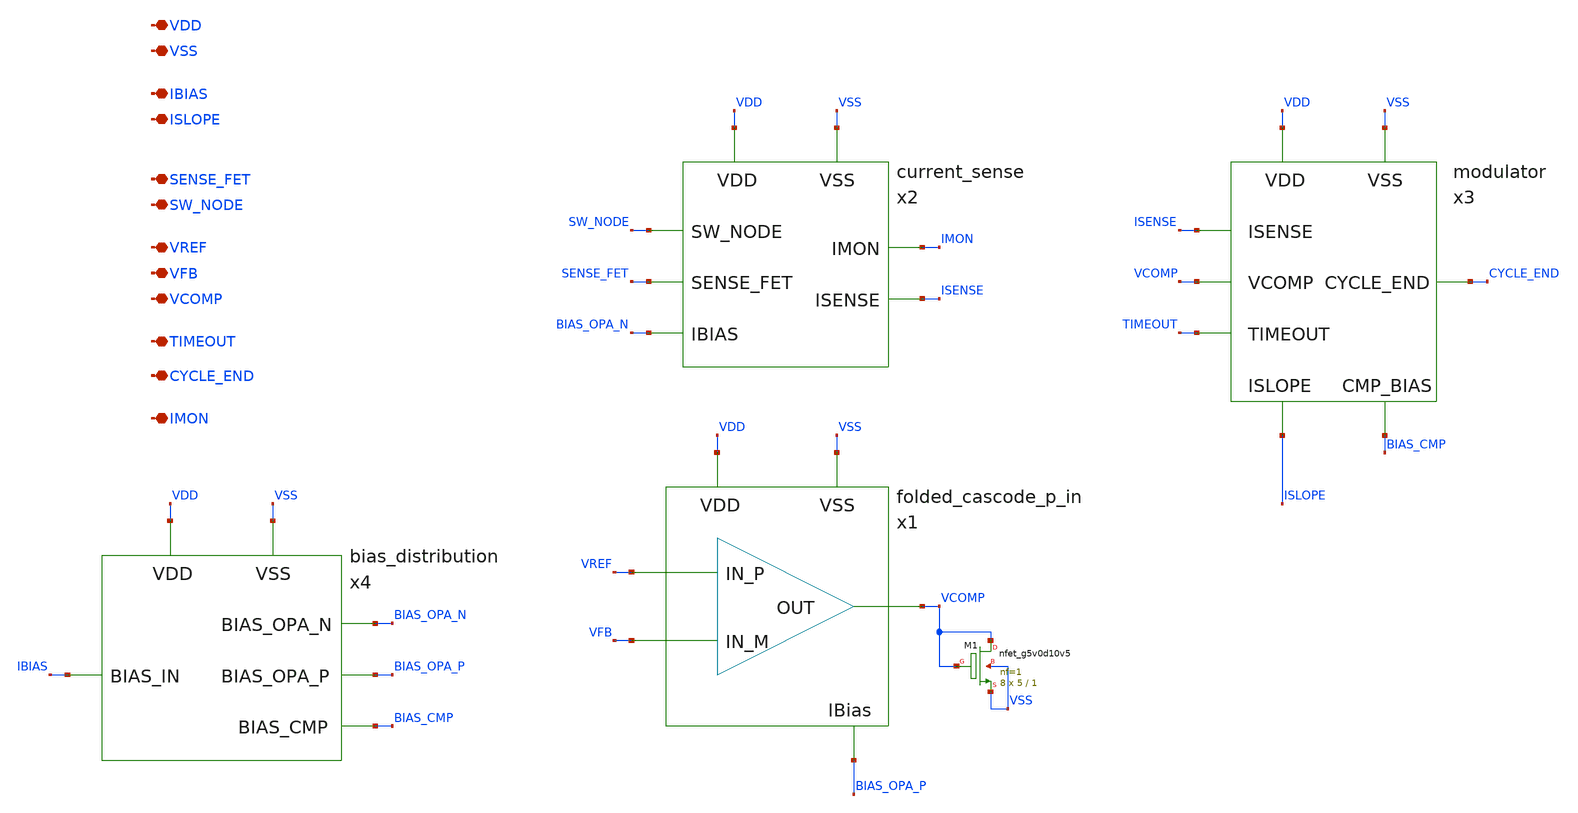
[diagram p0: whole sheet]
** sch_path: design/system/analog_subsystem.sch
**.subckt analog_subsystem VDD VSS IBIAS SENSE_FET SW_NODE ISLOPE VREF VFB VCOMP TIMEOUT CYCLE_END
*+ IMON
*.iopin VDD
*.iopin VSS
*.iopin IBIAS
*.iopin SENSE_FET
*.iopin SW_NODE
*.iopin ISLOPE
*.iopin VREF
*.iopin VFB
*.iopin VCOMP
*.iopin TIMEOUT
*.iopin CYCLE_END
*.iopin IMON
x1 VREF VFB VCOMP VDD VSS BIAS_OPA_P folded_cascode_p_in
x2 VDD VSS SW_NODE SENSE_FET BIAS_OPA_N IMON ISENSE current_sense
x3 VDD VSS BIAS_CMP ISLOPE ISENSE VCOMP TIMEOUT CYCLE_END modulator
x4 VDD VSS IBIAS BIAS_OPA_N BIAS_OPA_P BIAS_CMP bias_distribution
XM1 VCOMP VCOMP VSS VSS sky130_fd_pr__nfet_g5v0d10v5 L=1 W=5 nf=1 ad='int((nf+1)/2) * W/nf * 0.29' as='int((nf+2)/2) * W/nf * 0.29'
+ pd='2*int((nf+1)/2) * (W/nf + 0.29)' ps='2*int((nf+2)/2) * (W/nf + 0.29)' nrd='0.29 / W' nrs='0.29 / W'
+ sa=0 sb=0 sd=0 mult=8 m=8
**.ends

* expanding   symbol:  design/folded-cascode-p-in/folded_cascode_p_in.sym # of pins=6
** sym_path: design/folded-cascode-p-in/folded_cascode_p_in.sym
** sch_path: design/folded-cascode-p-in/folded_cascode_p_in.sch
.subckt folded_cascode_p_in IN_P IN_M OUT VDD VSS VBN
*.ipin IN_P
*.ipin IN_M
*.ipin OUT
*.ipin VDD
*.ipin VSS
*.ipin VBN
XM7 net4 VBP VDD VDD sky130_fd_pr__pfet_g5v0d10v5 L=1 W=5 nf=1 ad='int((nf+1)/2) * W/nf * 0.29' as='int((nf+2)/2) * W/nf * 0.29'
+ pd='2*int((nf+1)/2) * (W/nf + 0.29)' ps='2*int((nf+2)/2) * (W/nf + 0.29)' nrd='0.29 / W' nrs='0.29 / W'
+ sa=0 sb=0 sd=0 mult=12 m=12
XM8 VS1_P IN_M net4 VDD sky130_fd_pr__pfet_g5v0d10v5 L=1 W=5 nf=1 ad='int((nf+1)/2) * W/nf * 0.29' as='int((nf+2)/2) * W/nf * 0.29'
+ pd='2*int((nf+1)/2) * (W/nf + 0.29)' ps='2*int((nf+2)/2) * (W/nf + 0.29)' nrd='0.29 / W' nrs='0.29 / W'
+ sa=0 sb=0 sd=0 mult=24 m=24
XM15 VS1_M IN_P net4 VDD sky130_fd_pr__pfet_g5v0d10v5 L=1 W=5 nf=1 ad='int((nf+1)/2) * W/nf * 0.29' as='int((nf+2)/2) * W/nf * 0.29'
+ pd='2*int((nf+1)/2) * (W/nf + 0.29)' ps='2*int((nf+2)/2) * (W/nf + 0.29)' nrd='0.29 / W' nrs='0.29 / W'
+ sa=0 sb=0 sd=0 mult=24 m=24
XM16 VS1_P VBN_INT VSS VSS sky130_fd_pr__nfet_g5v0d10v5 L=1 W=5 nf=1 ad='int((nf+1)/2) * W/nf * 0.29'
+ as='int((nf+2)/2) * W/nf * 0.29' pd='2*int((nf+1)/2) * (W/nf + 0.29)' ps='2*int((nf+2)/2) * (W/nf + 0.29)'
+ nrd='0.29 / W' nrs='0.29 / W' sa=0 sb=0 sd=0 mult=10 m=10
XM20 VS1_M VBN_INT VSS VSS sky130_fd_pr__nfet_g5v0d10v5 L=1 W=5 nf=1 ad='int((nf+1)/2) * W/nf * 0.29'
+ as='int((nf+2)/2) * W/nf * 0.29' pd='2*int((nf+1)/2) * (W/nf + 0.29)' ps='2*int((nf+2)/2) * (W/nf + 0.29)'
+ nrd='0.29 / W' nrs='0.29 / W' sa=0 sb=0 sd=0 mult=10 m=10
XM22 net3 VCP net1 VDD sky130_fd_pr__pfet_g5v0d10v5 L=1 W=5 nf=1 ad='int((nf+1)/2) * W/nf * 0.29' as='int((nf+2)/2) * W/nf * 0.29'
+ pd='2*int((nf+1)/2) * (W/nf + 0.29)' ps='2*int((nf+2)/2) * (W/nf + 0.29)' nrd='0.29 / W' nrs='0.29 / W'
+ sa=0 sb=0 sd=0 mult=4 m=4
XM23 net1 net3 VDD VDD sky130_fd_pr__pfet_g5v0d10v5 L=1 W=5 nf=1 ad='int((nf+1)/2) * W/nf * 0.29' as='int((nf+2)/2) * W/nf * 0.29'
+ pd='2*int((nf+1)/2) * (W/nf + 0.29)' ps='2*int((nf+2)/2) * (W/nf + 0.29)' nrd='0.29 / W' nrs='0.29 / W'
+ sa=0 sb=0 sd=0 mult=4 m=4
XM24 OUT VCP net2 VDD sky130_fd_pr__pfet_g5v0d10v5 L=1 W=5 nf=1 ad='int((nf+1)/2) * W/nf * 0.29' as='int((nf+2)/2) * W/nf * 0.29'
+ pd='2*int((nf+1)/2) * (W/nf + 0.29)' ps='2*int((nf+2)/2) * (W/nf + 0.29)' nrd='0.29 / W' nrs='0.29 / W'
+ sa=0 sb=0 sd=0 mult=4 m=4
XM25 net2 net3 VDD VDD sky130_fd_pr__pfet_g5v0d10v5 L=1 W=5 nf=1 ad='int((nf+1)/2) * W/nf * 0.29' as='int((nf+2)/2) * W/nf * 0.29'
+ pd='2*int((nf+1)/2) * (W/nf + 0.29)' ps='2*int((nf+2)/2) * (W/nf + 0.29)' nrd='0.29 / W' nrs='0.29 / W'
+ sa=0 sb=0 sd=0 mult=4 m=4
XM26 OUT VCN VS1_P VSS sky130_fd_pr__nfet_g5v0d10v5 L=1 W=5 nf=1 ad='int((nf+1)/2) * W/nf * 0.29' as='int((nf+2)/2) * W/nf * 0.29'
+ pd='2*int((nf+1)/2) * (W/nf + 0.29)' ps='2*int((nf+2)/2) * (W/nf + 0.29)' nrd='0.29 / W' nrs='0.29 / W'
+ sa=0 sb=0 sd=0 mult=4 m=4
XM27 net3 VCN VS1_M VSS sky130_fd_pr__nfet_g5v0d10v5 L=1 W=5 nf=1 ad='int((nf+1)/2) * W/nf * 0.29' as='int((nf+2)/2) * W/nf * 0.29'
+ pd='2*int((nf+1)/2) * (W/nf + 0.29)' ps='2*int((nf+2)/2) * (W/nf + 0.29)' nrd='0.29 / W' nrs='0.29 / W'
+ sa=0 sb=0 sd=0 mult=4 m=4
XM29 VBN_INT VBN_INT VSS VSS sky130_fd_pr__nfet_g5v0d10v5 L=1 W=5 nf=1 ad='int((nf+1)/2) * W/nf * 0.29'
+ as='int((nf+2)/2) * W/nf * 0.29' pd='2*int((nf+1)/2) * (W/nf + 0.29)' ps='2*int((nf+2)/2) * (W/nf + 0.29)'
+ nrd='0.29 / W' nrs='0.29 / W' sa=0 sb=0 sd=0 mult=1 m=1
XM30 VBN_INT VBP VDD VDD sky130_fd_pr__pfet_g5v0d10v5 L=1 W=5 nf=1 ad='int((nf+1)/2) * W/nf * 0.29' as='int((nf+2)/2) * W/nf * 0.29'
+ pd='2*int((nf+1)/2) * (W/nf + 0.29)' ps='2*int((nf+2)/2) * (W/nf + 0.29)' nrd='0.29 / W' nrs='0.29 / W'
+ sa=0 sb=0 sd=0 mult=1 m=1
XM14 VBN_INT VBN_INT VS1_P VDD sky130_fd_pr__pfet_g5v0d10v5 L=1 W=5 nf=1 ad='int((nf+1)/2) * W/nf * 0.29'
+ as='int((nf+2)/2) * W/nf * 0.29' pd='2*int((nf+1)/2) * (W/nf + 0.29)' ps='2*int((nf+2)/2) * (W/nf + 0.29)'
+ nrd='0.29 / W' nrs='0.29 / W' sa=0 sb=0 sd=0 mult=1 m=1
XM17 VBN_INT VBN_INT VS1_M VDD sky130_fd_pr__pfet_g5v0d10v5 L=1 W=5 nf=1 ad='int((nf+1)/2) * W/nf * 0.29'
+ as='int((nf+2)/2) * W/nf * 0.29' pd='2*int((nf+1)/2) * (W/nf + 0.29)' ps='2*int((nf+2)/2) * (W/nf + 0.29)'
+ nrd='0.29 / W' nrs='0.29 / W' sa=0 sb=0 sd=0 mult=1 m=1
x1 VBN VCN VBP VCP VDD VSS cascode_bias
.ends


* expanding   symbol:  design/current-sense/current_sense.sym # of pins=7
** sym_path: design/current-sense/current_sense.sym
** sch_path: design/current-sense/current_sense.sch
.subckt current_sense VDD VSS SW_NODE SENSE_FET IBIAS IMON ISENSE
*.ipin SW_NODE
*.ipin SENSE_FET
*.ipin VDD
*.ipin VSS
*.ipin IBIAS
*.ipin IMON
*.ipin ISENSE
x1 SW_NODE SENSE_FET OPA_OUT VDD VSS IBIAS folded_cascode_n_in
XM1 net1 OPA_OUT SENSE_FET VDD sky130_fd_pr__pfet_g5v0d10v5 L=1 W=5 nf=1 ad='int((nf+1)/2) * W/nf * 0.29'
+ as='int((nf+2)/2) * W/nf * 0.29' pd='2*int((nf+1)/2) * (W/nf + 0.29)' ps='2*int((nf+2)/2) * (W/nf + 0.29)'
+ nrd='0.29 / W' nrs='0.29 / W' sa=0 sb=0 sd=0 mult=20 m=20
XM2 net1 net1 VSS VSS sky130_fd_pr__nfet_g5v0d10v5 L=1 W=5 nf=1 ad='int((nf+1)/2) * W/nf * 0.29' as='int((nf+2)/2) * W/nf * 0.29'
+ pd='2*int((nf+1)/2) * (W/nf + 0.29)' ps='2*int((nf+2)/2) * (W/nf + 0.29)' nrd='0.29 / W' nrs='0.29 / W'
+ sa=0 sb=0 sd=0 mult=20 m=20
XM4 net2 net1 VSS VSS sky130_fd_pr__nfet_g5v0d10v5 L=1 W=5 nf=1 ad='int((nf+1)/2) * W/nf * 0.29' as='int((nf+2)/2) * W/nf * 0.29'
+ pd='2*int((nf+1)/2) * (W/nf + 0.29)' ps='2*int((nf+2)/2) * (W/nf + 0.29)' nrd='0.29 / W' nrs='0.29 / W'
+ sa=0 sb=0 sd=0 mult=8 m=8
XM3 net2 net2 VDD VDD sky130_fd_pr__pfet_g5v0d10v5 L=1 W=5 nf=1 ad='int((nf+1)/2) * W/nf * 0.29' as='int((nf+2)/2) * W/nf * 0.29'
+ pd='2*int((nf+1)/2) * (W/nf + 0.29)' ps='2*int((nf+2)/2) * (W/nf + 0.29)' nrd='0.29 / W' nrs='0.29 / W'
+ sa=0 sb=0 sd=0 mult=8 m=8
XM5 I_MON net1 VSS VSS sky130_fd_pr__nfet_g5v0d10v5 L=1 W=5 nf=1 ad='int((nf+1)/2) * W/nf * 0.29' as='int((nf+2)/2) * W/nf * 0.29'
+ pd='2*int((nf+1)/2) * (W/nf + 0.29)' ps='2*int((nf+2)/2) * (W/nf + 0.29)' nrd='0.29 / W' nrs='0.29 / W'
+ sa=0 sb=0 sd=0 mult=20 m=20
XM6 ISENSE net2 VDD VDD sky130_fd_pr__pfet_g5v0d10v5 L=1 W=5 nf=1 ad='int((nf+1)/2) * W/nf * 0.29' as='int((nf+2)/2) * W/nf * 0.29'
+ pd='2*int((nf+1)/2) * (W/nf + 0.29)' ps='2*int((nf+2)/2) * (W/nf + 0.29)' nrd='0.29 / W' nrs='0.29 / W'
+ sa=0 sb=0 sd=0 mult=4 m=4
XR6 VSS ISENSE VSS sky130_fd_pr__res_high_po_1p41 L=20 mult=1 m=1
XR1 VSS ISENSE VSS sky130_fd_pr__res_high_po_1p41 L=20 mult=1 m=1
.ends


* expanding   symbol:  design/modulator/modulator.sym # of pins=8
** sym_path: design/modulator/modulator.sym
** sch_path: design/modulator/modulator.sch
.subckt modulator VDD VSS CMP_BIAS ISLOPE ISENSE VCOMP TIMEOUT CYCLE_END
*.ipin ISENSE
*.ipin VCOMP
*.ipin TIMEOUT
*.ipin VDD
*.ipin VSS
*.ipin CMP_BIAS
*.ipin ISLOPE
*.ipin CYCLE_END
x1 IMOD VCOMP CYCLE_END VDD VSS CMP_BIAS comparator_w_obuff
XM10 IMOD net1 VDD VDD sky130_fd_pr__pfet_g5v0d10v5 L=2 W=5 nf=1 ad='int((nf+1)/2) * W/nf * 0.29' as='int((nf+2)/2) * W/nf * 0.29'
+ pd='2*int((nf+1)/2) * (W/nf + 0.29)' ps='2*int((nf+2)/2) * (W/nf + 0.29)' nrd='0.29 / W' nrs='0.29 / W'
+ sa=0 sb=0 sd=0 mult=2 m=2
XM11 net1 net1 VDD VDD sky130_fd_pr__pfet_g5v0d10v5 L=2 W=5 nf=1 ad='int((nf+1)/2) * W/nf * 0.29' as='int((nf+2)/2) * W/nf * 0.29'
+ pd='2*int((nf+1)/2) * (W/nf + 0.29)' ps='2*int((nf+2)/2) * (W/nf + 0.29)' nrd='0.29 / W' nrs='0.29 / W'
+ sa=0 sb=0 sd=0 mult=12 m=12
XM12 ISENSE TIMEOUT VSS VSS sky130_fd_pr__nfet_g5v0d10v5 L=1 W=5 nf=1 ad='int((nf+1)/2) * W/nf * 0.29'
+ as='int((nf+2)/2) * W/nf * 0.29' pd='2*int((nf+1)/2) * (W/nf + 0.29)' ps='2*int((nf+2)/2) * (W/nf + 0.29)'
+ nrd='0.29 / W' nrs='0.29 / W' sa=0 sb=0 sd=0 mult=4 m=4
XM13 IMOD TIMEOUT ISENSE GND sky130_fd_pr__nfet_g5v0d10v5 L=1 W=5 nf=1 ad='int((nf+1)/2) * W/nf * 0.29'
+ as='int((nf+2)/2) * W/nf * 0.29' pd='2*int((nf+1)/2) * (W/nf + 0.29)' ps='2*int((nf+2)/2) * (W/nf + 0.29)'
+ nrd='0.29 / W' nrs='0.29 / W' sa=0 sb=0 sd=0 mult=1 m=1
XC4 IMOD ISENSE sky130_fd_pr__cap_mim_m3_1 W=30 L=30 MF=1 m=1
XC6 IMOD ISENSE sky130_fd_pr__cap_mim_m3_2 W=30 L=30 MF=1 m=1
XM1 net1 ISLOPE VSS VSS sky130_fd_pr__nfet_g5v0d10v5 L=1 W=5 nf=1 ad='int((nf+1)/2) * W/nf * 0.29' as='int((nf+2)/2) * W/nf * 0.29'
+ pd='2*int((nf+1)/2) * (W/nf + 0.29)' ps='2*int((nf+2)/2) * (W/nf + 0.29)' nrd='0.29 / W' nrs='0.29 / W'
+ sa=0 sb=0 sd=0 mult=1 m=1
XM2 ISLOPE ISLOPE VSS VSS sky130_fd_pr__nfet_g5v0d10v5 L=1 W=5 nf=1 ad='int((nf+1)/2) * W/nf * 0.29'
+ as='int((nf+2)/2) * W/nf * 0.29' pd='2*int((nf+1)/2) * (W/nf + 0.29)' ps='2*int((nf+2)/2) * (W/nf + 0.29)'
+ nrd='0.29 / W' nrs='0.29 / W' sa=0 sb=0 sd=0 mult=4 m=4
.ends


* expanding   symbol:  design/bias-circuit/bias_distribution.sym # of pins=6
** sym_path: design/bias-circuit/bias_distribution.sym
** sch_path: design/bias-circuit/bias_distribution.sch
.subckt bias_distribution VDD VSS BIAS_IN BIAS_OPA_N BIAS_OPA_P BIAS_CMP
*.ipin BIAS_OPA_P
*.ipin VSS
*.ipin VDD
*.ipin BIAS_IN
*.ipin BIAS_OPA_N
*.ipin BIAS_CMP
XM10 net1 net1 VDD VDD sky130_fd_pr__pfet_g5v0d10v5 L=2 W=5 nf=1 ad='int((nf+1)/2) * W/nf * 0.29' as='int((nf+2)/2) * W/nf * 0.29'
+ pd='2*int((nf+1)/2) * (W/nf + 0.29)' ps='2*int((nf+2)/2) * (W/nf + 0.29)' nrd='0.29 / W' nrs='0.29 / W'
+ sa=0 sb=0 sd=0 mult=2 m=2
XM13 BIAS_IN BIAS_IN VSS VSS sky130_fd_pr__nfet_g5v0d10v5 L=2 W=5 nf=1 ad='int((nf+1)/2) * W/nf * 0.29'
+ as='int((nf+2)/2) * W/nf * 0.29' pd='2*int((nf+1)/2) * (W/nf + 0.29)' ps='2*int((nf+2)/2) * (W/nf + 0.29)'
+ nrd='0.29 / W' nrs='0.29 / W' sa=0 sb=0 sd=0 mult=10 m=10
XM1 BIAS_CMP BIAS_IN VSS VSS sky130_fd_pr__nfet_g5v0d10v5 L=2 W=5 nf=1 ad='int((nf+1)/2) * W/nf * 0.29'
+ as='int((nf+2)/2) * W/nf * 0.29' pd='2*int((nf+1)/2) * (W/nf + 0.29)' ps='2*int((nf+2)/2) * (W/nf + 0.29)'
+ nrd='0.29 / W' nrs='0.29 / W' sa=0 sb=0 sd=0 mult=2 m=2
XM2 net1 BIAS_IN VSS VSS sky130_fd_pr__nfet_g5v0d10v5 L=2 W=5 nf=1 ad='int((nf+1)/2) * W/nf * 0.29' as='int((nf+2)/2) * W/nf * 0.29'
+ pd='2*int((nf+1)/2) * (W/nf + 0.29)' ps='2*int((nf+2)/2) * (W/nf + 0.29)' nrd='0.29 / W' nrs='0.29 / W'
+ sa=0 sb=0 sd=0 mult=2 m=2
XM3 BIAS_OPA_N net1 VDD VDD sky130_fd_pr__pfet_g5v0d10v5 L=2 W=5 nf=1 ad='int((nf+1)/2) * W/nf * 0.29'
+ as='int((nf+2)/2) * W/nf * 0.29' pd='2*int((nf+1)/2) * (W/nf + 0.29)' ps='2*int((nf+2)/2) * (W/nf + 0.29)'
+ nrd='0.29 / W' nrs='0.29 / W' sa=0 sb=0 sd=0 mult=2 m=2
XM4 BIAS_OPA_P net1 VDD VDD sky130_fd_pr__pfet_g5v0d10v5 L=2 W=5 nf=1 ad='int((nf+1)/2) * W/nf * 0.29'
+ as='int((nf+2)/2) * W/nf * 0.29' pd='2*int((nf+1)/2) * (W/nf + 0.29)' ps='2*int((nf+2)/2) * (W/nf + 0.29)'
+ nrd='0.29 / W' nrs='0.29 / W' sa=0 sb=0 sd=0 mult=2 m=2
.ends


* expanding   symbol:  design/bias-circuit/cascode_bias.sym # of pins=6
** sym_path: design/bias-circuit/cascode_bias.sym
** sch_path: design/bias-circuit/cascode_bias.sch
.subckt cascode_bias VBN VCN VBP VCP VDD VSS
*.ipin VCN
*.ipin VBP
*.ipin VCP
*.ipin VDD
*.ipin VSS
*.ipin VBN
XM1 VBP VBP VDD VDD sky130_fd_pr__pfet_g5v0d10v5 L=1 W=5 nf=1 ad='int((nf+1)/2) * W/nf * 0.29' as='int((nf+2)/2) * W/nf * 0.29'
+ pd='2*int((nf+1)/2) * (W/nf + 0.29)' ps='2*int((nf+2)/2) * (W/nf + 0.29)' nrd='0.29 / W' nrs='0.29 / W'
+ sa=0 sb=0 sd=0 mult=1 m=1
XM2 net1 VBP net8 VDD sky130_fd_pr__pfet_g5v0d10v5 L=1 W=5 nf=1 ad='int((nf+1)/2) * W/nf * 0.29' as='int((nf+2)/2) * W/nf * 0.29'
+ pd='2*int((nf+1)/2) * (W/nf + 0.29)' ps='2*int((nf+2)/2) * (W/nf + 0.29)' nrd='0.29 / W' nrs='0.29 / W'
+ sa=0 sb=0 sd=0 mult=1 m=1
XM3 VCN VBP VDD VDD sky130_fd_pr__pfet_g5v0d10v5 L=1 W=5 nf=1 ad='int((nf+1)/2) * W/nf * 0.29' as='int((nf+2)/2) * W/nf * 0.29'
+ pd='2*int((nf+1)/2) * (W/nf + 0.29)' ps='2*int((nf+2)/2) * (W/nf + 0.29)' nrd='0.29 / W' nrs='0.29 / W'
+ sa=0 sb=0 sd=0 mult=1 m=1
XM4 net1 net1 net2 VSS sky130_fd_pr__nfet_g5v0d10v5 L=1 W=5 nf=1 ad='int((nf+1)/2) * W/nf * 0.29' as='int((nf+2)/2) * W/nf * 0.29'
+ pd='2*int((nf+1)/2) * (W/nf + 0.29)' ps='2*int((nf+2)/2) * (W/nf + 0.29)' nrd='0.29 / W' nrs='0.29 / W'
+ sa=0 sb=0 sd=0 mult=2 m=2
XM5 net2 net1 VSS VSS sky130_fd_pr__nfet_g5v0d10v5 L=1 W=5 nf=1 ad='int((nf+1)/2) * W/nf * 0.29' as='int((nf+2)/2) * W/nf * 0.29'
+ pd='2*int((nf+1)/2) * (W/nf + 0.29)' ps='2*int((nf+2)/2) * (W/nf + 0.29)' nrd='0.29 / W' nrs='0.29 / W'
+ sa=0 sb=0 sd=0 mult=1 m=1
XM21 VCN VCN net2 VSS sky130_fd_pr__nfet_g5v0d10v5 L=1 W=5 nf=1 ad='int((nf+1)/2) * W/nf * 0.29' as='int((nf+2)/2) * W/nf * 0.29'
+ pd='2*int((nf+1)/2) * (W/nf + 0.29)' ps='2*int((nf+2)/2) * (W/nf + 0.29)' nrd='0.29 / W' nrs='0.29 / W'
+ sa=0 sb=0 sd=0 mult=1 m=1
XM6 net3 VBN net6 VSS sky130_fd_pr__nfet_g5v0d10v5 L=1 W=5 nf=1 ad='int((nf+1)/2) * W/nf * 0.29' as='int((nf+2)/2) * W/nf * 0.29'
+ pd='2*int((nf+1)/2) * (W/nf + 0.29)' ps='2*int((nf+2)/2) * (W/nf + 0.29)' nrd='0.29 / W' nrs='0.29 / W'
+ sa=0 sb=0 sd=0 mult=1 m=1
XM9 VCP VBN VSS VSS sky130_fd_pr__nfet_g5v0d10v5 L=1 W=5 nf=1 ad='int((nf+1)/2) * W/nf * 0.29' as='int((nf+2)/2) * W/nf * 0.29'
+ pd='2*int((nf+1)/2) * (W/nf + 0.29)' ps='2*int((nf+2)/2) * (W/nf + 0.29)' nrd='0.29 / W' nrs='0.29 / W'
+ sa=0 sb=0 sd=0 mult=1 m=1
XM10 net3 net3 net4 VDD sky130_fd_pr__pfet_g5v0d10v5 L=1 W=5 nf=1 ad='int((nf+1)/2) * W/nf * 0.29' as='int((nf+2)/2) * W/nf * 0.29'
+ pd='2*int((nf+1)/2) * (W/nf + 0.29)' ps='2*int((nf+2)/2) * (W/nf + 0.29)' nrd='0.29 / W' nrs='0.29 / W'
+ sa=0 sb=0 sd=0 mult=2 m=2
XM11 VCP VCP net4 VDD sky130_fd_pr__pfet_g5v0d10v5 L=1 W=5 nf=1 ad='int((nf+1)/2) * W/nf * 0.29' as='int((nf+2)/2) * W/nf * 0.29'
+ pd='2*int((nf+1)/2) * (W/nf + 0.29)' ps='2*int((nf+2)/2) * (W/nf + 0.29)' nrd='0.29 / W' nrs='0.29 / W'
+ sa=0 sb=0 sd=0 mult=1 m=1
XM28 net4 net3 VDD VDD sky130_fd_pr__pfet_g5v0d10v5 L=1 W=5 nf=1 ad='int((nf+1)/2) * W/nf * 0.29' as='int((nf+2)/2) * W/nf * 0.29'
+ pd='2*int((nf+1)/2) * (W/nf + 0.29)' ps='2*int((nf+2)/2) * (W/nf + 0.29)' nrd='0.29 / W' nrs='0.29 / W'
+ sa=0 sb=0 sd=0 mult=1 m=1
XM12 VBP VBN VSS VSS sky130_fd_pr__nfet_g5v0d10v5 L=1 W=5 nf=1 ad='int((nf+1)/2) * W/nf * 0.29' as='int((nf+2)/2) * W/nf * 0.29'
+ pd='2*int((nf+1)/2) * (W/nf + 0.29)' ps='2*int((nf+2)/2) * (W/nf + 0.29)' nrd='0.29 / W' nrs='0.29 / W'
+ sa=0 sb=0 sd=0 mult=1 m=1
XM32 net8 VBP net5 VDD sky130_fd_pr__pfet_g5v0d10v5 L=1 W=5 nf=1 ad='int((nf+1)/2) * W/nf * 0.29' as='int((nf+2)/2) * W/nf * 0.29'
+ pd='2*int((nf+1)/2) * (W/nf + 0.29)' ps='2*int((nf+2)/2) * (W/nf + 0.29)' nrd='0.29 / W' nrs='0.29 / W'
+ sa=0 sb=0 sd=0 mult=1 m=1
XM33 net5 VBP VDD VDD sky130_fd_pr__pfet_g5v0d10v5 L=1 W=5 nf=1 ad='int((nf+1)/2) * W/nf * 0.29' as='int((nf+2)/2) * W/nf * 0.29'
+ pd='2*int((nf+1)/2) * (W/nf + 0.29)' ps='2*int((nf+2)/2) * (W/nf + 0.29)' nrd='0.29 / W' nrs='0.29 / W'
+ sa=0 sb=0 sd=0 mult=1 m=1
XM34 net6 VBN net7 VSS sky130_fd_pr__nfet_g5v0d10v5 L=1 W=5 nf=1 ad='int((nf+1)/2) * W/nf * 0.29' as='int((nf+2)/2) * W/nf * 0.29'
+ pd='2*int((nf+1)/2) * (W/nf + 0.29)' ps='2*int((nf+2)/2) * (W/nf + 0.29)' nrd='0.29 / W' nrs='0.29 / W'
+ sa=0 sb=0 sd=0 mult=1 m=1
XM35 net7 VBN VSS VSS sky130_fd_pr__nfet_g5v0d10v5 L=1 W=5 nf=1 ad='int((nf+1)/2) * W/nf * 0.29' as='int((nf+2)/2) * W/nf * 0.29'
+ pd='2*int((nf+1)/2) * (W/nf + 0.29)' ps='2*int((nf+2)/2) * (W/nf + 0.29)' nrd='0.29 / W' nrs='0.29 / W'
+ sa=0 sb=0 sd=0 mult=1 m=1
XM13 VBN VBN VSS VSS sky130_fd_pr__nfet_g5v0d10v5 L=1 W=5 nf=1 ad='int((nf+1)/2) * W/nf * 0.29' as='int((nf+2)/2) * W/nf * 0.29'
+ pd='2*int((nf+1)/2) * (W/nf + 0.29)' ps='2*int((nf+2)/2) * (W/nf + 0.29)' nrd='0.29 / W' nrs='0.29 / W'
+ sa=0 sb=0 sd=0 mult=1 m=1
.ends


* expanding   symbol:  design/folded-cascode-n-in/folded_cascode_n_in.sym # of pins=6
** sym_path: design/folded-cascode-n-in/folded_cascode_n_in.sym
** sch_path: design/folded-cascode-n-in/folded_cascode_n_in.sch
.subckt folded_cascode_n_in IN_P IN_M OUT VDD VSS VBN
*.ipin IN_P
*.ipin IN_M
*.ipin OUT
*.ipin VDD
*.ipin VSS
*.ipin VBN
XM1 net1 VBN VSS VSS sky130_fd_pr__nfet_g5v0d10v5 L=1 W=5 nf=1 ad='int((nf+1)/2) * W/nf * 0.29' as='int((nf+2)/2) * W/nf * 0.29'
+ pd='2*int((nf+1)/2) * (W/nf + 0.29)' ps='2*int((nf+2)/2) * (W/nf + 0.29)' nrd='0.29 / W' nrs='0.29 / W'
+ sa=0 sb=0 sd=0 mult=12 m=12
XM3 VS1_P IN_M net1 VSS sky130_fd_pr__nfet_g5v0d10v5 L=1 W=5 nf=1 ad='int((nf+1)/2) * W/nf * 0.29' as='int((nf+2)/2) * W/nf * 0.29'
+ pd='2*int((nf+1)/2) * (W/nf + 0.29)' ps='2*int((nf+2)/2) * (W/nf + 0.29)' nrd='0.29 / W' nrs='0.29 / W'
+ sa=0 sb=0 sd=0 mult=24 m=24
XM4 VS1_M IN_P net1 VSS sky130_fd_pr__nfet_g5v0d10v5 L=1 W=5 nf=1 ad='int((nf+1)/2) * W/nf * 0.29' as='int((nf+2)/2) * W/nf * 0.29'
+ pd='2*int((nf+1)/2) * (W/nf + 0.29)' ps='2*int((nf+2)/2) * (W/nf + 0.29)' nrd='0.29 / W' nrs='0.29 / W'
+ sa=0 sb=0 sd=0 mult=24 m=24
XM9 net2 VCN net4 VSS sky130_fd_pr__nfet_g5v0d10v5 L=1 W=5 nf=1 ad='int((nf+1)/2) * W/nf * 0.29' as='int((nf+2)/2) * W/nf * 0.29'
+ pd='2*int((nf+1)/2) * (W/nf + 0.29)' ps='2*int((nf+2)/2) * (W/nf + 0.29)' nrd='0.29 / W' nrs='0.29 / W'
+ sa=0 sb=0 sd=0 mult=4 m=4
XM10 net3 net2 VSS VSS sky130_fd_pr__nfet_g5v0d10v5 L=1 W=5 nf=1 ad='int((nf+1)/2) * W/nf * 0.29' as='int((nf+2)/2) * W/nf * 0.29'
+ pd='2*int((nf+1)/2) * (W/nf + 0.29)' ps='2*int((nf+2)/2) * (W/nf + 0.29)' nrd='0.29 / W' nrs='0.29 / W'
+ sa=0 sb=0 sd=0 mult=4 m=4
XM11 net4 net2 VSS VSS sky130_fd_pr__nfet_g5v0d10v5 L=1 W=5 nf=1 ad='int((nf+1)/2) * W/nf * 0.29' as='int((nf+2)/2) * W/nf * 0.29'
+ pd='2*int((nf+1)/2) * (W/nf + 0.29)' ps='2*int((nf+2)/2) * (W/nf + 0.29)' nrd='0.29 / W' nrs='0.29 / W'
+ sa=0 sb=0 sd=0 mult=4 m=4
XM12 OUT VCN net3 VSS sky130_fd_pr__nfet_g5v0d10v5 L=1 W=5 nf=1 ad='int((nf+1)/2) * W/nf * 0.29' as='int((nf+2)/2) * W/nf * 0.29'
+ pd='2*int((nf+1)/2) * (W/nf + 0.29)' ps='2*int((nf+2)/2) * (W/nf + 0.29)' nrd='0.29 / W' nrs='0.29 / W'
+ sa=0 sb=0 sd=0 mult=4 m=4
XM5 VS1_P VBP_INT VDD VDD sky130_fd_pr__pfet_g5v0d10v5 L=1 W=5 nf=1 ad='int((nf+1)/2) * W/nf * 0.29'
+ as='int((nf+2)/2) * W/nf * 0.29' pd='2*int((nf+1)/2) * (W/nf + 0.29)' ps='2*int((nf+2)/2) * (W/nf + 0.29)'
+ nrd='0.29 / W' nrs='0.29 / W' sa=0 sb=0 sd=0 mult=10 m=10
XM13 VS1_M VBP_INT VDD VDD sky130_fd_pr__pfet_g5v0d10v5 L=1 W=5 nf=1 ad='int((nf+1)/2) * W/nf * 0.29'
+ as='int((nf+2)/2) * W/nf * 0.29' pd='2*int((nf+1)/2) * (W/nf + 0.29)' ps='2*int((nf+2)/2) * (W/nf + 0.29)'
+ nrd='0.29 / W' nrs='0.29 / W' sa=0 sb=0 sd=0 mult=10 m=10
XM17 VBP_INT VBN VSS VSS sky130_fd_pr__nfet_g5v0d10v5 L=1 W=5 nf=1 ad='int((nf+1)/2) * W/nf * 0.29' as='int((nf+2)/2) * W/nf * 0.29'
+ pd='2*int((nf+1)/2) * (W/nf + 0.29)' ps='2*int((nf+2)/2) * (W/nf + 0.29)' nrd='0.29 / W' nrs='0.29 / W'
+ sa=0 sb=0 sd=0 mult=1 m=1
XM18 VBP_INT VBP_INT VDD VDD sky130_fd_pr__pfet_g5v0d10v5 L=1 W=5 nf=1 ad='int((nf+1)/2) * W/nf * 0.29'
+ as='int((nf+2)/2) * W/nf * 0.29' pd='2*int((nf+1)/2) * (W/nf + 0.29)' ps='2*int((nf+2)/2) * (W/nf + 0.29)'
+ nrd='0.29 / W' nrs='0.29 / W' sa=0 sb=0 sd=0 mult=1 m=1
XM14 net2 VCP VS1_M VDD sky130_fd_pr__pfet_g5v0d10v5 L=1 W=5 nf=1 ad='int((nf+1)/2) * W/nf * 0.29' as='int((nf+2)/2) * W/nf * 0.29'
+ pd='2*int((nf+1)/2) * (W/nf + 0.29)' ps='2*int((nf+2)/2) * (W/nf + 0.29)' nrd='0.29 / W' nrs='0.29 / W'
+ sa=0 sb=0 sd=0 mult=4 m=4
XM19 OUT VCP VS1_P VDD sky130_fd_pr__pfet_g5v0d10v5 L=1 W=5 nf=1 ad='int((nf+1)/2) * W/nf * 0.29' as='int((nf+2)/2) * W/nf * 0.29'
+ pd='2*int((nf+1)/2) * (W/nf + 0.29)' ps='2*int((nf+2)/2) * (W/nf + 0.29)' nrd='0.29 / W' nrs='0.29 / W'
+ sa=0 sb=0 sd=0 mult=4 m=4
XM2 VBP_INT VBP_INT VS1_P VSS sky130_fd_pr__nfet_g5v0d10v5 L=1 W=5 nf=1 ad='int((nf+1)/2) * W/nf * 0.29'
+ as='int((nf+2)/2) * W/nf * 0.29' pd='2*int((nf+1)/2) * (W/nf + 0.29)' ps='2*int((nf+2)/2) * (W/nf + 0.29)'
+ nrd='0.29 / W' nrs='0.29 / W' sa=0 sb=0 sd=0 mult=1 m=1
XM6 VBP_INT VBP_INT VS1_M VSS sky130_fd_pr__nfet_g5v0d10v5 L=1 W=5 nf=1 ad='int((nf+1)/2) * W/nf * 0.29'
+ as='int((nf+2)/2) * W/nf * 0.29' pd='2*int((nf+1)/2) * (W/nf + 0.29)' ps='2*int((nf+2)/2) * (W/nf + 0.29)'
+ nrd='0.29 / W' nrs='0.29 / W' sa=0 sb=0 sd=0 mult=1 m=1
XM7 VBP VBP VDD VDD sky130_fd_pr__pfet_g5v0d10v5 L=1 W=5 nf=1 ad='int((nf+1)/2) * W/nf * 0.29' as='int((nf+2)/2) * W/nf * 0.29'
+ pd='2*int((nf+1)/2) * (W/nf + 0.29)' ps='2*int((nf+2)/2) * (W/nf + 0.29)' nrd='0.29 / W' nrs='0.29 / W'
+ sa=0 sb=0 sd=0 mult=1 m=1
XM8 net5 VBP net12 VDD sky130_fd_pr__pfet_g5v0d10v5 L=1 W=5 nf=1 ad='int((nf+1)/2) * W/nf * 0.29' as='int((nf+2)/2) * W/nf * 0.29'
+ pd='2*int((nf+1)/2) * (W/nf + 0.29)' ps='2*int((nf+2)/2) * (W/nf + 0.29)' nrd='0.29 / W' nrs='0.29 / W'
+ sa=0 sb=0 sd=0 mult=1 m=1
XM15 VCN VBP VDD VDD sky130_fd_pr__pfet_g5v0d10v5 L=1 W=5 nf=1 ad='int((nf+1)/2) * W/nf * 0.29' as='int((nf+2)/2) * W/nf * 0.29'
+ pd='2*int((nf+1)/2) * (W/nf + 0.29)' ps='2*int((nf+2)/2) * (W/nf + 0.29)' nrd='0.29 / W' nrs='0.29 / W'
+ sa=0 sb=0 sd=0 mult=1 m=1
XM16 net5 net5 net6 VSS sky130_fd_pr__nfet_g5v0d10v5 L=1 W=5 nf=1 ad='int((nf+1)/2) * W/nf * 0.29' as='int((nf+2)/2) * W/nf * 0.29'
+ pd='2*int((nf+1)/2) * (W/nf + 0.29)' ps='2*int((nf+2)/2) * (W/nf + 0.29)' nrd='0.29 / W' nrs='0.29 / W'
+ sa=0 sb=0 sd=0 mult=2 m=2
XM20 net6 net5 VSS VSS sky130_fd_pr__nfet_g5v0d10v5 L=1 W=5 nf=1 ad='int((nf+1)/2) * W/nf * 0.29' as='int((nf+2)/2) * W/nf * 0.29'
+ pd='2*int((nf+1)/2) * (W/nf + 0.29)' ps='2*int((nf+2)/2) * (W/nf + 0.29)' nrd='0.29 / W' nrs='0.29 / W'
+ sa=0 sb=0 sd=0 mult=1 m=1
XM21 VCN VCN net6 VSS sky130_fd_pr__nfet_g5v0d10v5 L=1 W=5 nf=1 ad='int((nf+1)/2) * W/nf * 0.29' as='int((nf+2)/2) * W/nf * 0.29'
+ pd='2*int((nf+1)/2) * (W/nf + 0.29)' ps='2*int((nf+2)/2) * (W/nf + 0.29)' nrd='0.29 / W' nrs='0.29 / W'
+ sa=0 sb=0 sd=0 mult=1 m=1
XM24 net7 VBN net10 VSS sky130_fd_pr__nfet_g5v0d10v5 L=1 W=5 nf=1 ad='int((nf+1)/2) * W/nf * 0.29' as='int((nf+2)/2) * W/nf * 0.29'
+ pd='2*int((nf+1)/2) * (W/nf + 0.29)' ps='2*int((nf+2)/2) * (W/nf + 0.29)' nrd='0.29 / W' nrs='0.29 / W'
+ sa=0 sb=0 sd=0 mult=1 m=1
XM25 VCP VBN VSS VSS sky130_fd_pr__nfet_g5v0d10v5 L=1 W=5 nf=1 ad='int((nf+1)/2) * W/nf * 0.29' as='int((nf+2)/2) * W/nf * 0.29'
+ pd='2*int((nf+1)/2) * (W/nf + 0.29)' ps='2*int((nf+2)/2) * (W/nf + 0.29)' nrd='0.29 / W' nrs='0.29 / W'
+ sa=0 sb=0 sd=0 mult=1 m=1
XM26 net7 net7 net8 VDD sky130_fd_pr__pfet_g5v0d10v5 L=1 W=5 nf=1 ad='int((nf+1)/2) * W/nf * 0.29' as='int((nf+2)/2) * W/nf * 0.29'
+ pd='2*int((nf+1)/2) * (W/nf + 0.29)' ps='2*int((nf+2)/2) * (W/nf + 0.29)' nrd='0.29 / W' nrs='0.29 / W'
+ sa=0 sb=0 sd=0 mult=2 m=2
XM27 VCP VCP net8 VDD sky130_fd_pr__pfet_g5v0d10v5 L=1 W=5 nf=1 ad='int((nf+1)/2) * W/nf * 0.29' as='int((nf+2)/2) * W/nf * 0.29'
+ pd='2*int((nf+1)/2) * (W/nf + 0.29)' ps='2*int((nf+2)/2) * (W/nf + 0.29)' nrd='0.29 / W' nrs='0.29 / W'
+ sa=0 sb=0 sd=0 mult=1 m=1
XM28 net8 net7 VDD VDD sky130_fd_pr__pfet_g5v0d10v5 L=1 W=5 nf=1 ad='int((nf+1)/2) * W/nf * 0.29' as='int((nf+2)/2) * W/nf * 0.29'
+ pd='2*int((nf+1)/2) * (W/nf + 0.29)' ps='2*int((nf+2)/2) * (W/nf + 0.29)' nrd='0.29 / W' nrs='0.29 / W'
+ sa=0 sb=0 sd=0 mult=1 m=1
XM29 VBP VBN VSS VSS sky130_fd_pr__nfet_g5v0d10v5 L=1 W=5 nf=1 ad='int((nf+1)/2) * W/nf * 0.29' as='int((nf+2)/2) * W/nf * 0.29'
+ pd='2*int((nf+1)/2) * (W/nf + 0.29)' ps='2*int((nf+2)/2) * (W/nf + 0.29)' nrd='0.29 / W' nrs='0.29 / W'
+ sa=0 sb=0 sd=0 mult=1 m=1
XM32 net12 VBP net9 VDD sky130_fd_pr__pfet_g5v0d10v5 L=1 W=5 nf=1 ad='int((nf+1)/2) * W/nf * 0.29' as='int((nf+2)/2) * W/nf * 0.29'
+ pd='2*int((nf+1)/2) * (W/nf + 0.29)' ps='2*int((nf+2)/2) * (W/nf + 0.29)' nrd='0.29 / W' nrs='0.29 / W'
+ sa=0 sb=0 sd=0 mult=1 m=1
XM33 net9 VBP VDD VDD sky130_fd_pr__pfet_g5v0d10v5 L=1 W=5 nf=1 ad='int((nf+1)/2) * W/nf * 0.29' as='int((nf+2)/2) * W/nf * 0.29'
+ pd='2*int((nf+1)/2) * (W/nf + 0.29)' ps='2*int((nf+2)/2) * (W/nf + 0.29)' nrd='0.29 / W' nrs='0.29 / W'
+ sa=0 sb=0 sd=0 mult=1 m=1
XM34 net10 VBN net11 VSS sky130_fd_pr__nfet_g5v0d10v5 L=1 W=5 nf=1 ad='int((nf+1)/2) * W/nf * 0.29' as='int((nf+2)/2) * W/nf * 0.29'
+ pd='2*int((nf+1)/2) * (W/nf + 0.29)' ps='2*int((nf+2)/2) * (W/nf + 0.29)' nrd='0.29 / W' nrs='0.29 / W'
+ sa=0 sb=0 sd=0 mult=1 m=1
XM35 net11 VBN VSS VSS sky130_fd_pr__nfet_g5v0d10v5 L=1 W=5 nf=1 ad='int((nf+1)/2) * W/nf * 0.29' as='int((nf+2)/2) * W/nf * 0.29'
+ pd='2*int((nf+1)/2) * (W/nf + 0.29)' ps='2*int((nf+2)/2) * (W/nf + 0.29)' nrd='0.29 / W' nrs='0.29 / W'
+ sa=0 sb=0 sd=0 mult=1 m=1
XM30 VBN VBN VSS VSS sky130_fd_pr__nfet_g5v0d10v5 L=1 W=5 nf=1 ad='int((nf+1)/2) * W/nf * 0.29' as='int((nf+2)/2) * W/nf * 0.29'
+ pd='2*int((nf+1)/2) * (W/nf + 0.29)' ps='2*int((nf+2)/2) * (W/nf + 0.29)' nrd='0.29 / W' nrs='0.29 / W'
+ sa=0 sb=0 sd=0 mult=1 m=1
.ends


* expanding   symbol:  design/comparator/comparator_w_obuff.sym # of pins=6
** sym_path: design/comparator/comparator_w_obuff.sym
** sch_path: design/comparator/comparator_w_obuff.sch
.subckt comparator_w_obuff Vinp Vinm Vout VDD VSS IB
*.iopin VDD
*.iopin VSS
*.iopin Vout
*.iopin Vinp
*.iopin Vinm
*.iopin IB
XM11 net4 IB VDD VDD sky130_fd_pr__pfet_g5v0d10v5 L=1 W=5 nf=1 ad='int((nf+1)/2) * W/nf * 0.29' as='int((nf+2)/2) * W/nf * 0.29'
+ pd='2*int((nf+1)/2) * (W/nf + 0.29)' ps='2*int((nf+2)/2) * (W/nf + 0.29)' nrd='0.29 / W' nrs='0.29 / W'
+ sa=0 sb=0 sd=0 mult=4 m=4
XM8 VMID net1 VDD VDD sky130_fd_pr__pfet_g5v0d10v5 L=1 W=5 nf=1 ad='int((nf+1)/2) * W/nf * 0.29' as='int((nf+2)/2) * W/nf * 0.29'
+ pd='2*int((nf+1)/2) * (W/nf + 0.29)' ps='2*int((nf+2)/2) * (W/nf + 0.29)' nrd='0.29 / W' nrs='0.29 / W'
+ sa=0 sb=0 sd=0 mult=4 m=4
XM7 net1 net1 VDD VDD sky130_fd_pr__pfet_g5v0d10v5 L=1 W=5 nf=1 ad='int((nf+1)/2) * W/nf * 0.29' as='int((nf+2)/2) * W/nf * 0.29'
+ pd='2*int((nf+1)/2) * (W/nf + 0.29)' ps='2*int((nf+2)/2) * (W/nf + 0.29)' nrd='0.29 / W' nrs='0.29 / W'
+ sa=0 sb=0 sd=0 mult=4 m=4
XM2 net3 Vinm net4 VDD sky130_fd_pr__pfet_g5v0d10v5 L=1 W=5 nf=1 ad='int((nf+1)/2) * W/nf * 0.29' as='int((nf+2)/2) * W/nf * 0.29'
+ pd='2*int((nf+1)/2) * (W/nf + 0.29)' ps='2*int((nf+2)/2) * (W/nf + 0.29)' nrd='0.29 / W' nrs='0.29 / W'
+ sa=0 sb=0 sd=0 mult=4 m=4
XM1 net2 Vinp net4 VDD sky130_fd_pr__pfet_g5v0d10v5 L=1 W=5 nf=1 ad='int((nf+1)/2) * W/nf * 0.29' as='int((nf+2)/2) * W/nf * 0.29'
+ pd='2*int((nf+1)/2) * (W/nf + 0.29)' ps='2*int((nf+2)/2) * (W/nf + 0.29)' nrd='0.29 / W' nrs='0.29 / W'
+ sa=0 sb=0 sd=0 mult=4 m=4
XMmir IB IB VDD VDD sky130_fd_pr__pfet_g5v0d10v5 L=1 W=5 nf=1 ad='int((nf+1)/2) * W/nf * 0.29' as='int((nf+2)/2) * W/nf * 0.29'
+ pd='2*int((nf+1)/2) * (W/nf + 0.29)' ps='2*int((nf+2)/2) * (W/nf + 0.29)' nrd='0.29 / W' nrs='0.29 / W'
+ sa=0 sb=0 sd=0 mult=2 m=2
XM12 VMID net3 VSS VSS sky130_fd_pr__nfet_g5v0d10v5 L=1 W=5 nf=1 ad='int((nf+1)/2) * W/nf * 0.29' as='int((nf+2)/2) * W/nf * 0.29'
+ pd='2*int((nf+1)/2) * (W/nf + 0.29)' ps='2*int((nf+2)/2) * (W/nf + 0.29)' nrd='0.29 / W' nrs='0.29 / W'
+ sa=0 sb=0 sd=0 mult=4 m=4
XM4 net3 net3 VSS VSS sky130_fd_pr__nfet_g5v0d10v5 L=1 W=5 nf=1 ad='int((nf+1)/2) * W/nf * 0.29' as='int((nf+2)/2) * W/nf * 0.29'
+ pd='2*int((nf+1)/2) * (W/nf + 0.29)' ps='2*int((nf+2)/2) * (W/nf + 0.29)' nrd='0.29 / W' nrs='0.29 / W'
+ sa=0 sb=0 sd=0 mult=3 m=3
XM6 net2 net3 VSS VSS sky130_fd_pr__nfet_g5v0d10v5 L=1 W=5 nf=1 ad='int((nf+1)/2) * W/nf * 0.29' as='int((nf+2)/2) * W/nf * 0.29'
+ pd='2*int((nf+1)/2) * (W/nf + 0.29)' ps='2*int((nf+2)/2) * (W/nf + 0.29)' nrd='0.29 / W' nrs='0.29 / W'
+ sa=0 sb=0 sd=0 mult=4 m=4
XM5 net3 net2 VSS VSS sky130_fd_pr__nfet_g5v0d10v5 L=1 W=5 nf=1 ad='int((nf+1)/2) * W/nf * 0.29' as='int((nf+2)/2) * W/nf * 0.29'
+ pd='2*int((nf+1)/2) * (W/nf + 0.29)' ps='2*int((nf+2)/2) * (W/nf + 0.29)' nrd='0.29 / W' nrs='0.29 / W'
+ sa=0 sb=0 sd=0 mult=4 m=4
XM3 net2 net2 VSS VSS sky130_fd_pr__nfet_g5v0d10v5 L=1 W=5 nf=1 ad='int((nf+1)/2) * W/nf * 0.29' as='int((nf+2)/2) * W/nf * 0.29'
+ pd='2*int((nf+1)/2) * (W/nf + 0.29)' ps='2*int((nf+2)/2) * (W/nf + 0.29)' nrd='0.29 / W' nrs='0.29 / W'
+ sa=0 sb=0 sd=0 mult=3 m=3
XM9 net1 net2 VSS VSS sky130_fd_pr__nfet_g5v0d10v5 L=1 W=5 nf=1 ad='int((nf+1)/2) * W/nf * 0.29' as='int((nf+2)/2) * W/nf * 0.29'
+ pd='2*int((nf+1)/2) * (W/nf + 0.29)' ps='2*int((nf+2)/2) * (W/nf + 0.29)' nrd='0.29 / W' nrs='0.29 / W'
+ sa=0 sb=0 sd=0 mult=4 m=4
XM10 Vout VMID VDD VDD sky130_fd_pr__pfet_g5v0d10v5 L=0.5 W=5 nf=1 ad='int((nf+1)/2) * W/nf * 0.29' as='int((nf+2)/2) * W/nf * 0.29'
+ pd='2*int((nf+1)/2) * (W/nf + 0.29)' ps='2*int((nf+2)/2) * (W/nf + 0.29)' nrd='0.29 / W' nrs='0.29 / W'
+ sa=0 sb=0 sd=0 mult=1 m=1
XM13 Vout VMID VSS VSS sky130_fd_pr__nfet_g5v0d10v5 L=0.5 W=5 nf=1 ad='int((nf+1)/2) * W/nf * 0.29' as='int((nf+2)/2) * W/nf * 0.29'
+ pd='2*int((nf+1)/2) * (W/nf + 0.29)' ps='2*int((nf+2)/2) * (W/nf + 0.29)' nrd='0.29 / W' nrs='0.29 / W'
+ sa=0 sb=0 sd=0 mult=1 m=1
.ends

.GLOBAL GND
.end
